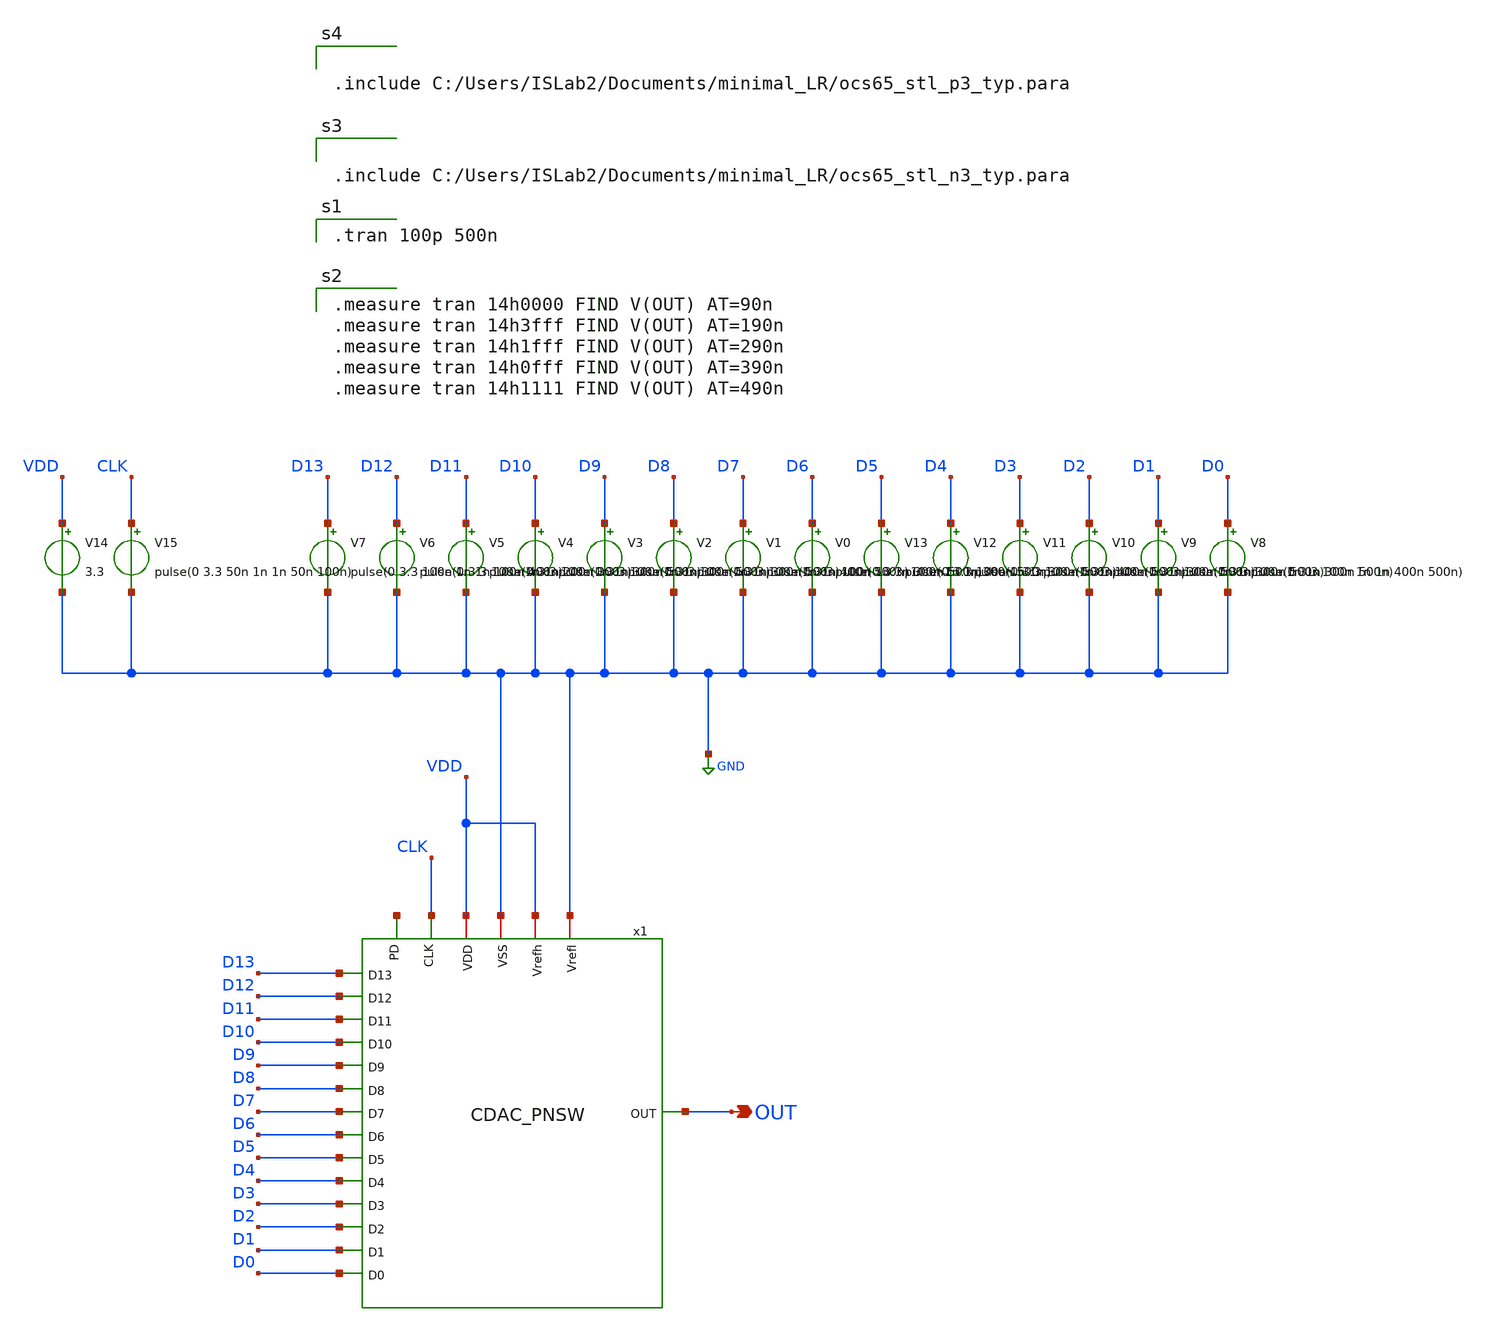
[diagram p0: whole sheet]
** sch_path: CDAC_sim.sch
**.subckt CDAC_sim OUT
*.opin OUT
V14 VDD GND 3.3
V15 CLK GND pulse(0 3.3 50n 1n 1n 50n 100n)
V13 D5 GND pulse(0 3.3 100n 1n 1n 300n 500n)
V12 D4 GND pulse(0 3.3 100n 1n 1n 400n 500n)
V11 D3 GND pulse(0 3.3 100n 1n 1n 300n 500n)
V10 D2 GND pulse(0 3.3 100n 1n 1n 300n 500n)
V9 D1 GND pulse(0 3.3 100n 1n 1n 300n 500n)
V8 D0 GND pulse(0 3.3 100n 1n 1n 400n 500n)
V7 D13 GND pulse(0 3.3 100n 1n 1n 100n 400n)
V6 D12 GND pulse(0 3.3 100n 1n 1n 200n 300n)
V5 D11 GND pulse(0 3.3 100n 1n 1n 300n 500n)
V4 D10 GND pulse(0 3.3 100n 1n 1n 300n 500n)
V3 D9 GND pulse(0 3.3 100n 1n 1n 300n 500n)
V2 D8 GND pulse(0 3.3 100n 1n 1n 400n 500n)
V1 D7 GND pulse(0 3.3 100n 1n 1n 300n 500n)
V0 D6 GND pulse(0 3.3 100n 1n 1n 300n 500n)
x1 CLK D11 D13 D12 D7 D10 D1 D0 D9 D8 D2 D6 D5 D4 D3 OUT GND VDD GND VDD net1 CDAC_PNSW
**** begin user architecture code

.tran 100p 500n


.measure tran 14h0000 FIND V(OUT) AT=90n
.measure tran 14h3fff FIND V(OUT) AT=190n
.measure tran 14h1fff FIND V(OUT) AT=290n
.measure tran 14h0fff FIND V(OUT) AT=390n
.measure tran 14h1111 FIND V(OUT) AT=490n



.include C:/Users/ISLab2/Documents/minimal_LR/ocs65_stl_n3_typ.para



.include C:/Users/ISLab2/Documents/minimal_LR/ocs65_stl_p3_typ.para

**** end user architecture code
**.ends
.GLOBAL GND
.end
